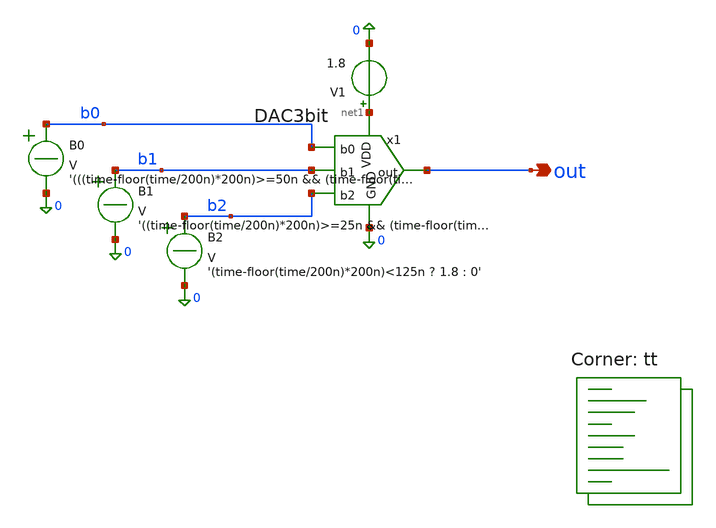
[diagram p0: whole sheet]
** sch_path: xschem/DAC3bit_tb.sch
**.subckt DAC3bit_tb out
*.opin out
B0 b0 0 V = '(((time-floor(time/200n)*200n)>=50n && (time-floor(time/200n)*200n)<75n) || ((time-floor(time/200n)*200n)>=125n && (time-floor(time/200n)*200n)<150n) || ((time-floor(time/200n)*200n)>=175n && (time-floor(time/200n)*200n)<200n)) ? 1.8 : 0'
B1 b1 0 V = '((time-floor(time/200n)*200n)>=25n && (time-floor(time/200n)*200n)<100n) ? 1.8 : 0'
B2 b2 0 V = '(time-floor(time/200n)*200n)<125n ? 1.8 : 0'
x1 b0 b1 b2 net1 out 0 DAC3bit
V1 net1 0 1.8
**** begin user architecture code
.lib $::SKYWATER_MODELS/sky130.lib.spice tt


.control
save all
tran 1n 5u
write DAC3bit_tran.raw
op
write DAC3bit_op.raw
ac dec 20 1k 100meg
write DAC3bit_ac.raw
.endc

**** end user architecture code
**.ends

* expanding   symbol:  DAC3bit.sym # of pins=6
** sym_path: xschem/DAC3bit.sym
** sch_path: xschem/DAC3bit.sch
.subckt DAC3bit b0 b1 b2 VDD out GND
*.opin out
*.ipin b0
*.ipin b1
*.ipin b2
*.ipin GND
*.ipin VDD
XR1 GND net3 sky130_fd_pr__res_generic_po W=1 L=21 m=1
XR2 net3 net1 sky130_fd_pr__res_generic_po W=1 L=21 m=1
XR3 b0 net4 sky130_fd_pr__res_generic_po W=1 L=21 m=1
XR4 net4 net1 sky130_fd_pr__res_generic_po W=1 L=21 m=1
XR5 b1 net5 sky130_fd_pr__res_generic_po W=1 L=21 m=1
XR6 net5 net2 sky130_fd_pr__res_generic_po W=1 L=21 m=1
XR7 b2 net6 sky130_fd_pr__res_generic_po W=1 L=21 m=1
XR8 net6 vx sky130_fd_pr__res_generic_po W=1 L=21 m=1
XR9 net1 net2 sky130_fd_pr__res_generic_po W=1 L=21 m=1
XR10 net2 vx sky130_fd_pr__res_generic_po W=1 L=21 m=1
XR12 VDD out sky130_fd_pr__res_generic_po W=1 L=21 m=1
XR13 out GND sky130_fd_pr__res_generic_po W=1 L=21 m=1
XR11 out vx sky130_fd_pr__res_generic_po W=1 L=63 m=1
.ends

.end
